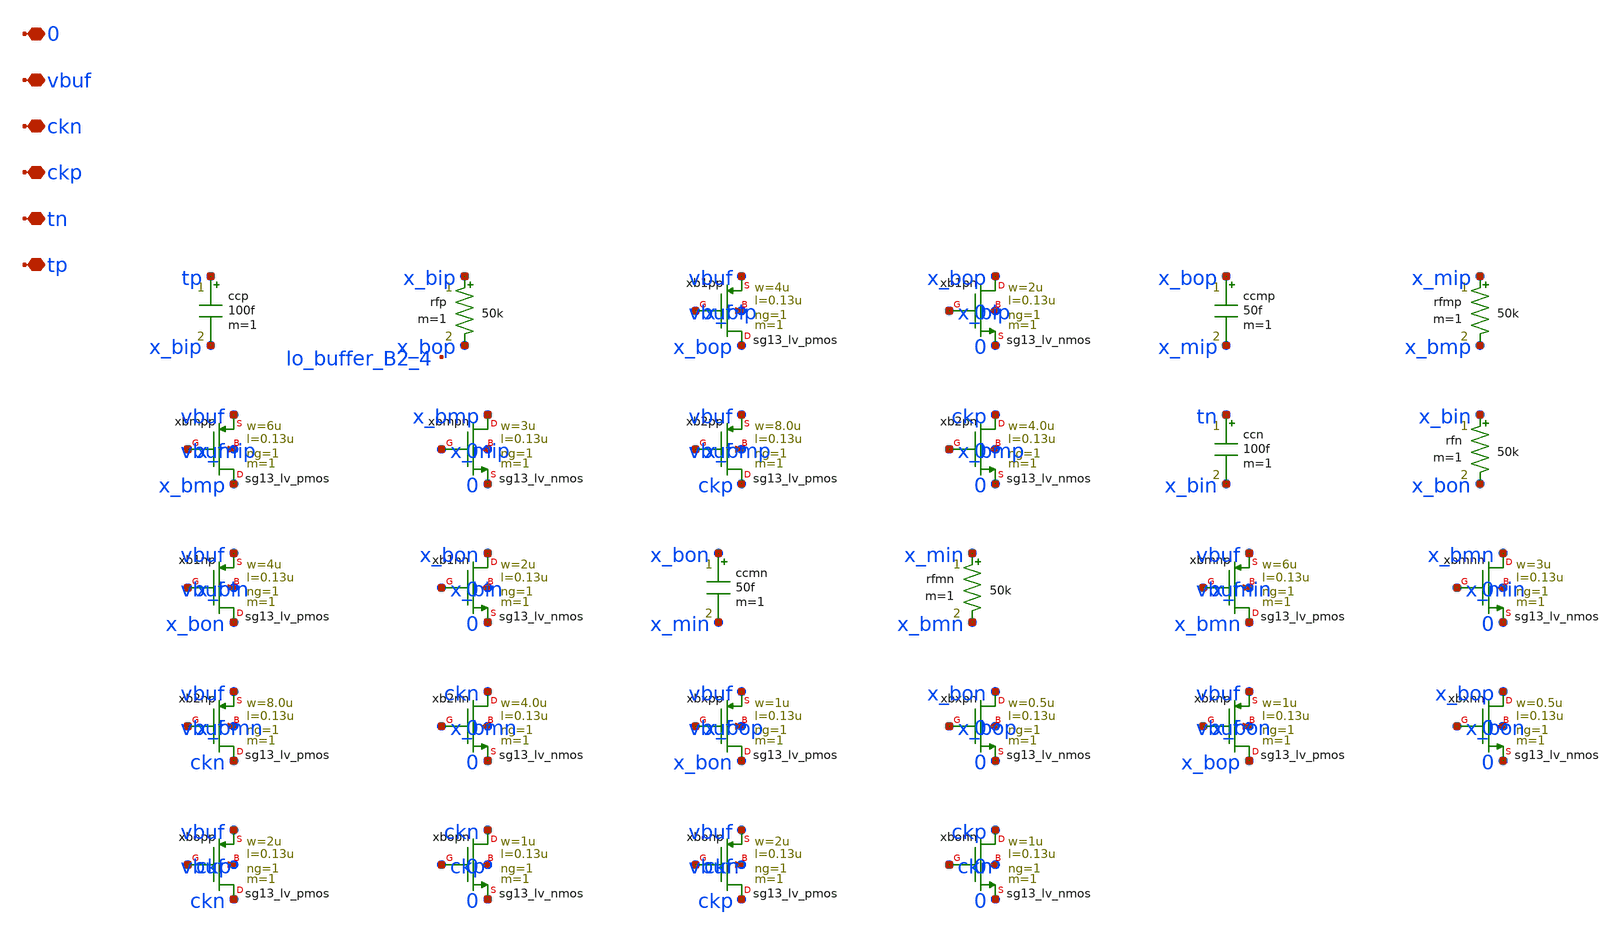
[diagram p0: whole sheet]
** sch_path: analog/lo/sch/lo_buffer.sch
**.subckt lo_buffer tp tn ckp ckn vbuf 0
*.iopin tp
*.iopin tn
*.iopin ckp
*.iopin ckn
*.iopin vbuf
*.iopin 0
ccp tp x_bip 100f m=1
rfp x_bip x_bop 50k m=1
Xxb1pp x_bop x_bip vbuf vbuf sg13_lv_pmos w=4u l=0.13u ng=1 m=1 mm_ok=1
Xxb1pn x_bop x_bip 0 0 sg13_lv_nmos w=2u l=0.13u ng=1 m=1 mm_ok=1
ccmp x_bop x_mip 50f m=1
rfmp x_mip x_bmp 50k m=1
Xxbmpp x_bmp x_mip vbuf vbuf sg13_lv_pmos w=6u l=0.13u ng=1 m=1 mm_ok=1
Xxbmpn x_bmp x_mip 0 0 sg13_lv_nmos w=3u l=0.13u ng=1 m=1 mm_ok=1
Xxb2pp ckp x_bmp vbuf vbuf sg13_lv_pmos w=8.0u l=0.13u ng=1 m=1 mm_ok=1
Xxb2pn ckp x_bmp 0 0 sg13_lv_nmos w=4.0u l=0.13u ng=1 m=1 mm_ok=1
ccn tn x_bin 100f m=1
rfn x_bin x_bon 50k m=1
Xxb1np x_bon x_bin vbuf vbuf sg13_lv_pmos w=4u l=0.13u ng=1 m=1 mm_ok=1
Xxb1nn x_bon x_bin 0 0 sg13_lv_nmos w=2u l=0.13u ng=1 m=1 mm_ok=1
ccmn x_bon x_min 50f m=1
rfmn x_min x_bmn 50k m=1
Xxbmnp x_bmn x_min vbuf vbuf sg13_lv_pmos w=6u l=0.13u ng=1 m=1 mm_ok=1
Xxbmnn x_bmn x_min 0 0 sg13_lv_nmos w=3u l=0.13u ng=1 m=1 mm_ok=1
Xxb2np ckn x_bmn vbuf vbuf sg13_lv_pmos w=8.0u l=0.13u ng=1 m=1 mm_ok=1
Xxb2nn ckn x_bmn 0 0 sg13_lv_nmos w=4.0u l=0.13u ng=1 m=1 mm_ok=1
Xxbxpp x_bon x_bop vbuf vbuf sg13_lv_pmos w=1u l=0.13u ng=1 m=1 mm_ok=1
Xxbxpn x_bon x_bop 0 0 sg13_lv_nmos w=0.5u l=0.13u ng=1 m=1 mm_ok=1
Xxbxnp x_bop x_bon vbuf vbuf sg13_lv_pmos w=1u l=0.13u ng=1 m=1 mm_ok=1
Xxbxnn x_bop x_bon 0 0 sg13_lv_nmos w=0.5u l=0.13u ng=1 m=1 mm_ok=1
Xxbopp ckn ckp vbuf vbuf sg13_lv_pmos w=2u l=0.13u ng=1 m=1 mm_ok=1
Xxbopn ckn ckp 0 0 sg13_lv_nmos w=1u l=0.13u ng=1 m=1 mm_ok=1
Xxbonp ckp ckn vbuf vbuf sg13_lv_pmos w=2u l=0.13u ng=1 m=1 mm_ok=1
Xxbonn ckp ckn 0 0 sg13_lv_nmos w=1u l=0.13u ng=1 m=1 mm_ok=1
**.ends
.end
